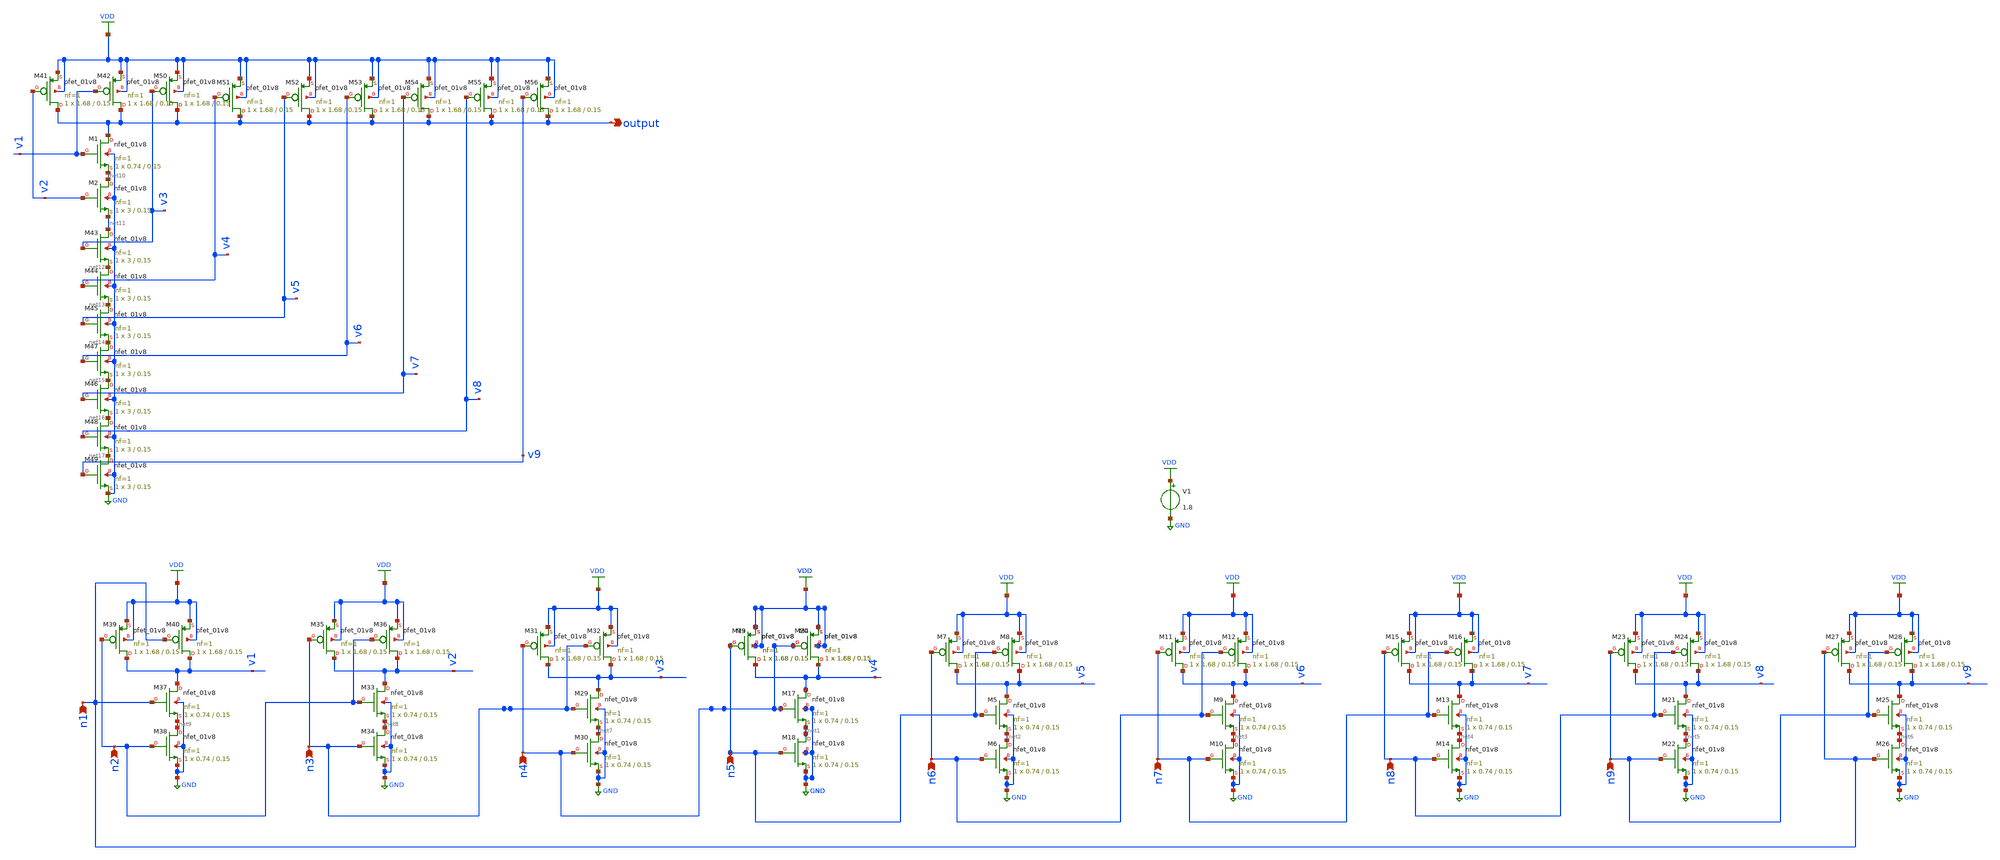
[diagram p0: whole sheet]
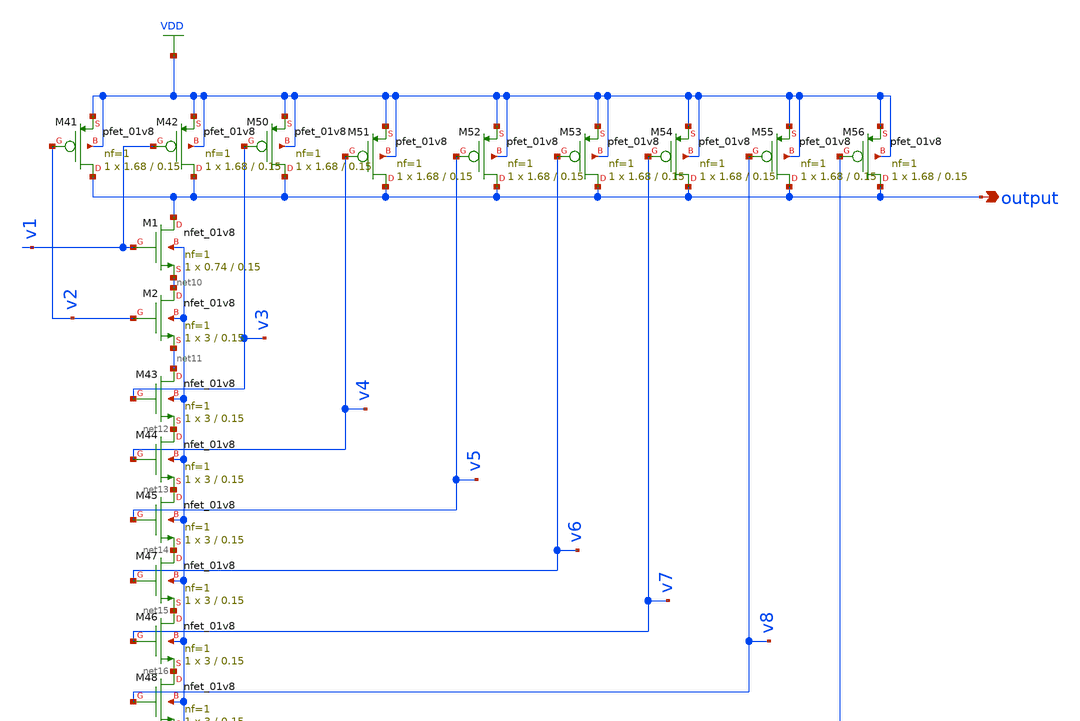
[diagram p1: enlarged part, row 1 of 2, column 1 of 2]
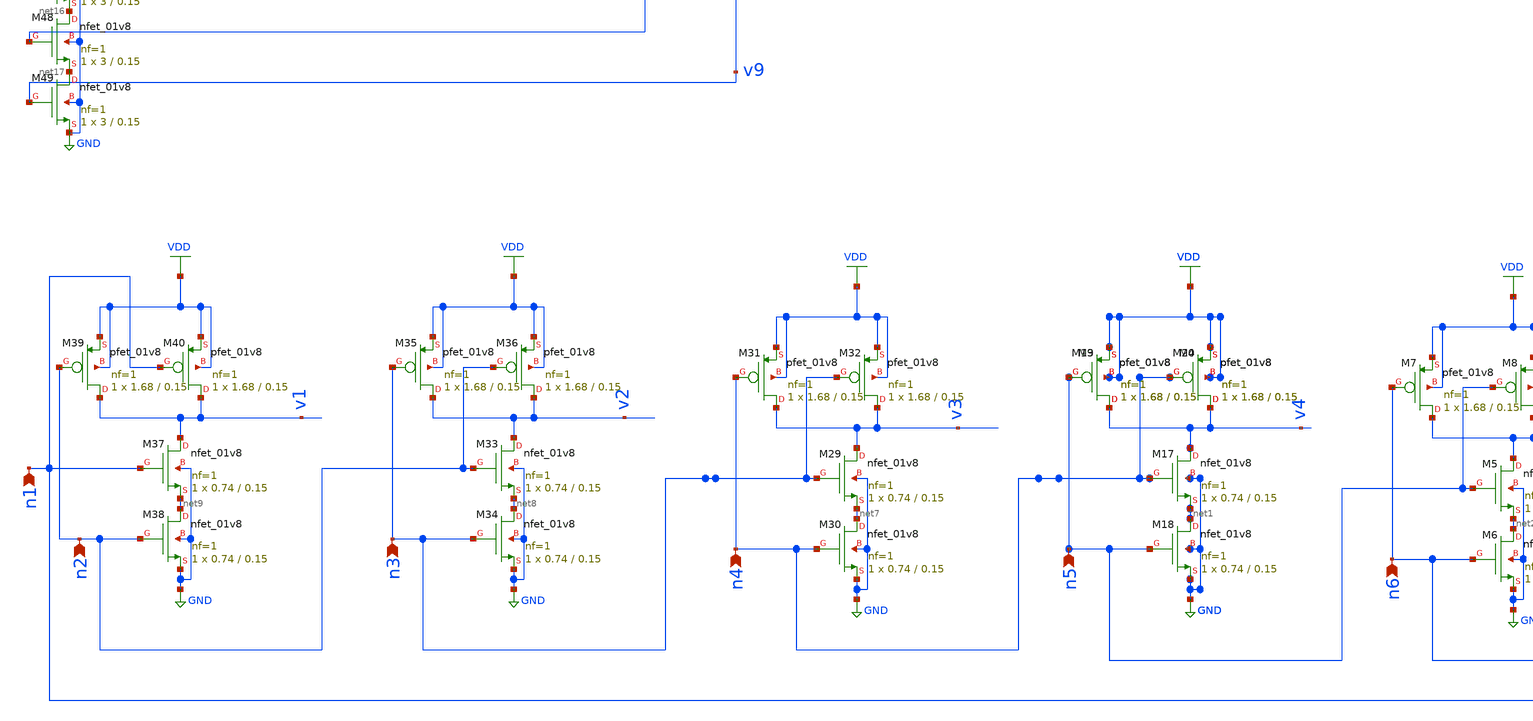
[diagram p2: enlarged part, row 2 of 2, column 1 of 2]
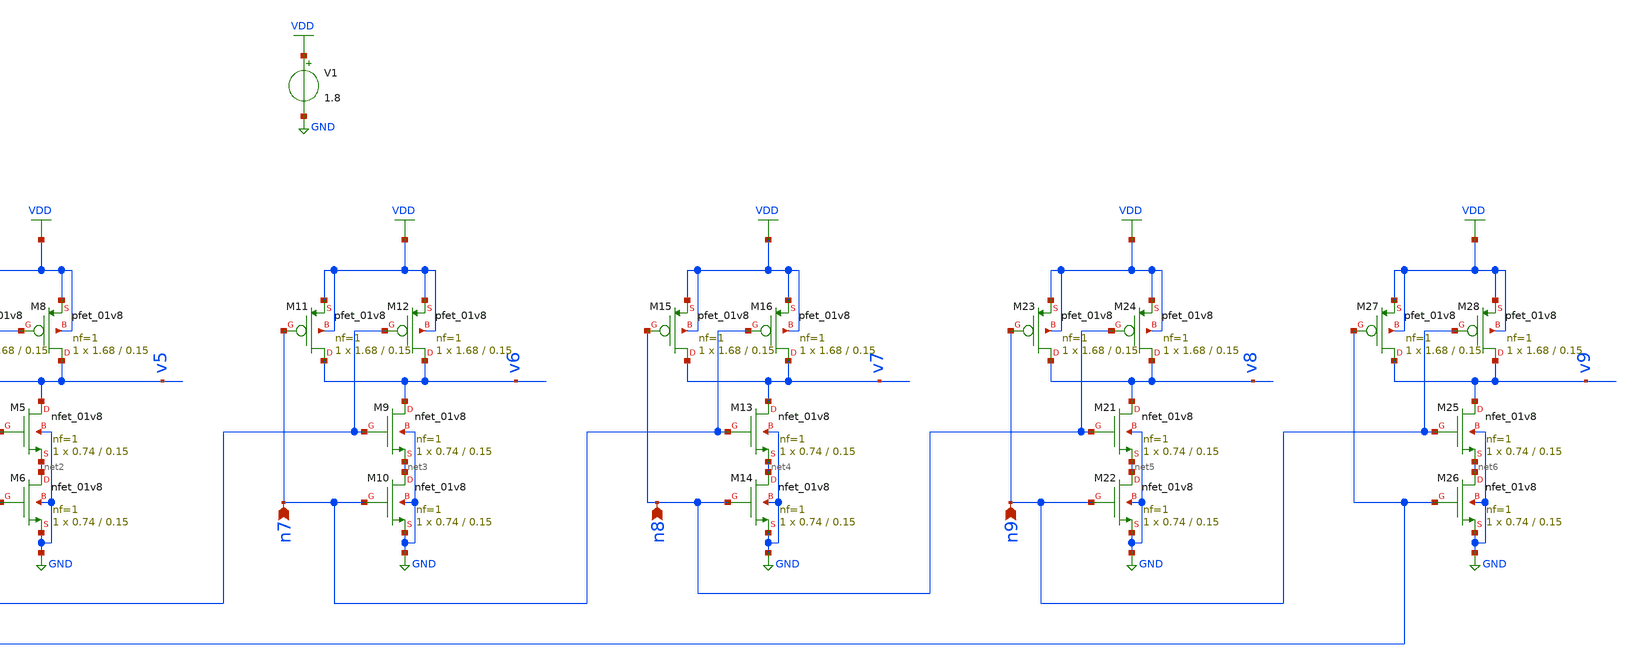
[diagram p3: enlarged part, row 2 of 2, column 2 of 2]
** sch_path: edgecombiner.sch
**.subckt edgecombiner n1 n2 n3 n4 n5 n6 n7 n8 n9 output
*.ipin n1
*.ipin n2
*.ipin n3
*.ipin n4
*.ipin n5
*.ipin n6
*.ipin n7
*.ipin n8
*.ipin n9
*.opin output
XM3 v4 n5 VDD VDD sky130_fd_pr__pfet_01v8 L=0.15 W=1.68 nf=1 ad='int((nf+1)/2) * W/nf * 0.29' as='int((nf+2)/2) * W/nf * 0.29'
+ pd='2*int((nf+1)/2) * (W/nf + 0.29)' ps='2*int((nf+2)/2) * (W/nf + 0.29)' nrd='0.29 / W' nrs='0.29 / W'
+ sa=0 sb=0 sd=0 mult=1 m=1
XM4 v4 n4 VDD VDD sky130_fd_pr__pfet_01v8 L=0.15 W=1.68 nf=1 ad='int((nf+1)/2) * W/nf * 0.29' as='int((nf+2)/2) * W/nf * 0.29'
+ pd='2*int((nf+1)/2) * (W/nf + 0.29)' ps='2*int((nf+2)/2) * (W/nf + 0.29)' nrd='0.29 / W' nrs='0.29 / W'
+ sa=0 sb=0 sd=0 mult=1 m=1
XM5 v5 n5 net2 GND sky130_fd_pr__nfet_01v8 L=0.15 W=0.74 nf=1 ad='int((nf+1)/2) * W/nf * 0.29' as='int((nf+2)/2) * W/nf * 0.29'
+ pd='2*int((nf+1)/2) * (W/nf + 0.29)' ps='2*int((nf+2)/2) * (W/nf + 0.29)' nrd='0.29 / W' nrs='0.29 / W'
+ sa=0 sb=0 sd=0 mult=1 m=1
XM6 net2 n6 GND GND sky130_fd_pr__nfet_01v8 L=0.15 W=0.74 nf=1 ad='int((nf+1)/2) * W/nf * 0.29' as='int((nf+2)/2) * W/nf * 0.29'
+ pd='2*int((nf+1)/2) * (W/nf + 0.29)' ps='2*int((nf+2)/2) * (W/nf + 0.29)' nrd='0.29 / W' nrs='0.29 / W'
+ sa=0 sb=0 sd=0 mult=1 m=1
XM7 v5 n6 VDD VDD sky130_fd_pr__pfet_01v8 L=0.15 W=1.68 nf=1 ad='int((nf+1)/2) * W/nf * 0.29' as='int((nf+2)/2) * W/nf * 0.29'
+ pd='2*int((nf+1)/2) * (W/nf + 0.29)' ps='2*int((nf+2)/2) * (W/nf + 0.29)' nrd='0.29 / W' nrs='0.29 / W'
+ sa=0 sb=0 sd=0 mult=1 m=1
XM8 v5 n5 VDD VDD sky130_fd_pr__pfet_01v8 L=0.15 W=1.68 nf=1 ad='int((nf+1)/2) * W/nf * 0.29' as='int((nf+2)/2) * W/nf * 0.29'
+ pd='2*int((nf+1)/2) * (W/nf + 0.29)' ps='2*int((nf+2)/2) * (W/nf + 0.29)' nrd='0.29 / W' nrs='0.29 / W'
+ sa=0 sb=0 sd=0 mult=1 m=1
XM9 v6 n6 net3 GND sky130_fd_pr__nfet_01v8 L=0.15 W=0.74 nf=1 ad='int((nf+1)/2) * W/nf * 0.29' as='int((nf+2)/2) * W/nf * 0.29'
+ pd='2*int((nf+1)/2) * (W/nf + 0.29)' ps='2*int((nf+2)/2) * (W/nf + 0.29)' nrd='0.29 / W' nrs='0.29 / W'
+ sa=0 sb=0 sd=0 mult=1 m=1
XM10 net3 n7 GND GND sky130_fd_pr__nfet_01v8 L=0.15 W=0.74 nf=1 ad='int((nf+1)/2) * W/nf * 0.29' as='int((nf+2)/2) * W/nf * 0.29'
+ pd='2*int((nf+1)/2) * (W/nf + 0.29)' ps='2*int((nf+2)/2) * (W/nf + 0.29)' nrd='0.29 / W' nrs='0.29 / W'
+ sa=0 sb=0 sd=0 mult=1 m=1
XM11 v6 n7 VDD VDD sky130_fd_pr__pfet_01v8 L=0.15 W=1.68 nf=1 ad='int((nf+1)/2) * W/nf * 0.29' as='int((nf+2)/2) * W/nf * 0.29'
+ pd='2*int((nf+1)/2) * (W/nf + 0.29)' ps='2*int((nf+2)/2) * (W/nf + 0.29)' nrd='0.29 / W' nrs='0.29 / W'
+ sa=0 sb=0 sd=0 mult=1 m=1
XM12 v6 n6 VDD VDD sky130_fd_pr__pfet_01v8 L=0.15 W=1.68 nf=1 ad='int((nf+1)/2) * W/nf * 0.29' as='int((nf+2)/2) * W/nf * 0.29'
+ pd='2*int((nf+1)/2) * (W/nf + 0.29)' ps='2*int((nf+2)/2) * (W/nf + 0.29)' nrd='0.29 / W' nrs='0.29 / W'
+ sa=0 sb=0 sd=0 mult=1 m=1
XM13 v7 n7 net4 GND sky130_fd_pr__nfet_01v8 L=0.15 W=0.74 nf=1 ad='int((nf+1)/2) * W/nf * 0.29' as='int((nf+2)/2) * W/nf * 0.29'
+ pd='2*int((nf+1)/2) * (W/nf + 0.29)' ps='2*int((nf+2)/2) * (W/nf + 0.29)' nrd='0.29 / W' nrs='0.29 / W'
+ sa=0 sb=0 sd=0 mult=1 m=1
XM14 net4 n8 GND GND sky130_fd_pr__nfet_01v8 L=0.15 W=0.74 nf=1 ad='int((nf+1)/2) * W/nf * 0.29' as='int((nf+2)/2) * W/nf * 0.29'
+ pd='2*int((nf+1)/2) * (W/nf + 0.29)' ps='2*int((nf+2)/2) * (W/nf + 0.29)' nrd='0.29 / W' nrs='0.29 / W'
+ sa=0 sb=0 sd=0 mult=1 m=1
XM15 v7 n8 VDD VDD sky130_fd_pr__pfet_01v8 L=0.15 W=1.68 nf=1 ad='int((nf+1)/2) * W/nf * 0.29' as='int((nf+2)/2) * W/nf * 0.29'
+ pd='2*int((nf+1)/2) * (W/nf + 0.29)' ps='2*int((nf+2)/2) * (W/nf + 0.29)' nrd='0.29 / W' nrs='0.29 / W'
+ sa=0 sb=0 sd=0 mult=1 m=1
XM16 v7 n7 VDD VDD sky130_fd_pr__pfet_01v8 L=0.15 W=1.68 nf=1 ad='int((nf+1)/2) * W/nf * 0.29' as='int((nf+2)/2) * W/nf * 0.29'
+ pd='2*int((nf+1)/2) * (W/nf + 0.29)' ps='2*int((nf+2)/2) * (W/nf + 0.29)' nrd='0.29 / W' nrs='0.29 / W'
+ sa=0 sb=0 sd=0 mult=1 m=1
XM17 v4 n4 net1 GND sky130_fd_pr__nfet_01v8 L=0.15 W=0.74 nf=1 ad='int((nf+1)/2) * W/nf * 0.29' as='int((nf+2)/2) * W/nf * 0.29'
+ pd='2*int((nf+1)/2) * (W/nf + 0.29)' ps='2*int((nf+2)/2) * (W/nf + 0.29)' nrd='0.29 / W' nrs='0.29 / W'
+ sa=0 sb=0 sd=0 mult=1 m=1
XM18 net1 n5 GND GND sky130_fd_pr__nfet_01v8 L=0.15 W=0.74 nf=1 ad='int((nf+1)/2) * W/nf * 0.29' as='int((nf+2)/2) * W/nf * 0.29'
+ pd='2*int((nf+1)/2) * (W/nf + 0.29)' ps='2*int((nf+2)/2) * (W/nf + 0.29)' nrd='0.29 / W' nrs='0.29 / W'
+ sa=0 sb=0 sd=0 mult=1 m=1
XM19 v4 n5 VDD VDD sky130_fd_pr__pfet_01v8 L=0.15 W=1.68 nf=1 ad='int((nf+1)/2) * W/nf * 0.29' as='int((nf+2)/2) * W/nf * 0.29'
+ pd='2*int((nf+1)/2) * (W/nf + 0.29)' ps='2*int((nf+2)/2) * (W/nf + 0.29)' nrd='0.29 / W' nrs='0.29 / W'
+ sa=0 sb=0 sd=0 mult=1 m=1
XM20 v4 n4 VDD VDD sky130_fd_pr__pfet_01v8 L=0.15 W=1.68 nf=1 ad='int((nf+1)/2) * W/nf * 0.29' as='int((nf+2)/2) * W/nf * 0.29'
+ pd='2*int((nf+1)/2) * (W/nf + 0.29)' ps='2*int((nf+2)/2) * (W/nf + 0.29)' nrd='0.29 / W' nrs='0.29 / W'
+ sa=0 sb=0 sd=0 mult=1 m=1
XM21 v8 n8 net5 GND sky130_fd_pr__nfet_01v8 L=0.15 W=0.74 nf=1 ad='int((nf+1)/2) * W/nf * 0.29' as='int((nf+2)/2) * W/nf * 0.29'
+ pd='2*int((nf+1)/2) * (W/nf + 0.29)' ps='2*int((nf+2)/2) * (W/nf + 0.29)' nrd='0.29 / W' nrs='0.29 / W'
+ sa=0 sb=0 sd=0 mult=1 m=1
XM22 net5 n9 GND GND sky130_fd_pr__nfet_01v8 L=0.15 W=0.74 nf=1 ad='int((nf+1)/2) * W/nf * 0.29' as='int((nf+2)/2) * W/nf * 0.29'
+ pd='2*int((nf+1)/2) * (W/nf + 0.29)' ps='2*int((nf+2)/2) * (W/nf + 0.29)' nrd='0.29 / W' nrs='0.29 / W'
+ sa=0 sb=0 sd=0 mult=1 m=1
XM23 v8 n9 VDD VDD sky130_fd_pr__pfet_01v8 L=0.15 W=1.68 nf=1 ad='int((nf+1)/2) * W/nf * 0.29' as='int((nf+2)/2) * W/nf * 0.29'
+ pd='2*int((nf+1)/2) * (W/nf + 0.29)' ps='2*int((nf+2)/2) * (W/nf + 0.29)' nrd='0.29 / W' nrs='0.29 / W'
+ sa=0 sb=0 sd=0 mult=1 m=1
XM24 v8 n8 VDD VDD sky130_fd_pr__pfet_01v8 L=0.15 W=1.68 nf=1 ad='int((nf+1)/2) * W/nf * 0.29' as='int((nf+2)/2) * W/nf * 0.29'
+ pd='2*int((nf+1)/2) * (W/nf + 0.29)' ps='2*int((nf+2)/2) * (W/nf + 0.29)' nrd='0.29 / W' nrs='0.29 / W'
+ sa=0 sb=0 sd=0 mult=1 m=1
XM25 v9 n9 net6 GND sky130_fd_pr__nfet_01v8 L=0.15 W=0.74 nf=1 ad='int((nf+1)/2) * W/nf * 0.29' as='int((nf+2)/2) * W/nf * 0.29'
+ pd='2*int((nf+1)/2) * (W/nf + 0.29)' ps='2*int((nf+2)/2) * (W/nf + 0.29)' nrd='0.29 / W' nrs='0.29 / W'
+ sa=0 sb=0 sd=0 mult=1 m=1
XM26 net6 n1 GND GND sky130_fd_pr__nfet_01v8 L=0.15 W=0.74 nf=1 ad='int((nf+1)/2) * W/nf * 0.29' as='int((nf+2)/2) * W/nf * 0.29'
+ pd='2*int((nf+1)/2) * (W/nf + 0.29)' ps='2*int((nf+2)/2) * (W/nf + 0.29)' nrd='0.29 / W' nrs='0.29 / W'
+ sa=0 sb=0 sd=0 mult=1 m=1
XM27 v9 n1 VDD VDD sky130_fd_pr__pfet_01v8 L=0.15 W=1.68 nf=1 ad='int((nf+1)/2) * W/nf * 0.29' as='int((nf+2)/2) * W/nf * 0.29'
+ pd='2*int((nf+1)/2) * (W/nf + 0.29)' ps='2*int((nf+2)/2) * (W/nf + 0.29)' nrd='0.29 / W' nrs='0.29 / W'
+ sa=0 sb=0 sd=0 mult=1 m=1
XM28 v9 n9 VDD VDD sky130_fd_pr__pfet_01v8 L=0.15 W=1.68 nf=1 ad='int((nf+1)/2) * W/nf * 0.29' as='int((nf+2)/2) * W/nf * 0.29'
+ pd='2*int((nf+1)/2) * (W/nf + 0.29)' ps='2*int((nf+2)/2) * (W/nf + 0.29)' nrd='0.29 / W' nrs='0.29 / W'
+ sa=0 sb=0 sd=0 mult=1 m=1
XM29 v3 n3 net7 GND sky130_fd_pr__nfet_01v8 L=0.15 W=0.74 nf=1 ad='int((nf+1)/2) * W/nf * 0.29' as='int((nf+2)/2) * W/nf * 0.29'
+ pd='2*int((nf+1)/2) * (W/nf + 0.29)' ps='2*int((nf+2)/2) * (W/nf + 0.29)' nrd='0.29 / W' nrs='0.29 / W'
+ sa=0 sb=0 sd=0 mult=1 m=1
XM30 net7 n4 GND GND sky130_fd_pr__nfet_01v8 L=0.15 W=0.74 nf=1 ad='int((nf+1)/2) * W/nf * 0.29' as='int((nf+2)/2) * W/nf * 0.29'
+ pd='2*int((nf+1)/2) * (W/nf + 0.29)' ps='2*int((nf+2)/2) * (W/nf + 0.29)' nrd='0.29 / W' nrs='0.29 / W'
+ sa=0 sb=0 sd=0 mult=1 m=1
XM31 v3 n4 VDD VDD sky130_fd_pr__pfet_01v8 L=0.15 W=1.68 nf=1 ad='int((nf+1)/2) * W/nf * 0.29' as='int((nf+2)/2) * W/nf * 0.29'
+ pd='2*int((nf+1)/2) * (W/nf + 0.29)' ps='2*int((nf+2)/2) * (W/nf + 0.29)' nrd='0.29 / W' nrs='0.29 / W'
+ sa=0 sb=0 sd=0 mult=1 m=1
XM32 v3 n3 VDD VDD sky130_fd_pr__pfet_01v8 L=0.15 W=1.68 nf=1 ad='int((nf+1)/2) * W/nf * 0.29' as='int((nf+2)/2) * W/nf * 0.29'
+ pd='2*int((nf+1)/2) * (W/nf + 0.29)' ps='2*int((nf+2)/2) * (W/nf + 0.29)' nrd='0.29 / W' nrs='0.29 / W'
+ sa=0 sb=0 sd=0 mult=1 m=1
XM33 v2 n2 net8 GND sky130_fd_pr__nfet_01v8 L=0.15 W=0.74 nf=1 ad='int((nf+1)/2) * W/nf * 0.29' as='int((nf+2)/2) * W/nf * 0.29'
+ pd='2*int((nf+1)/2) * (W/nf + 0.29)' ps='2*int((nf+2)/2) * (W/nf + 0.29)' nrd='0.29 / W' nrs='0.29 / W'
+ sa=0 sb=0 sd=0 mult=1 m=1
XM34 net8 n3 GND GND sky130_fd_pr__nfet_01v8 L=0.15 W=0.74 nf=1 ad='int((nf+1)/2) * W/nf * 0.29' as='int((nf+2)/2) * W/nf * 0.29'
+ pd='2*int((nf+1)/2) * (W/nf + 0.29)' ps='2*int((nf+2)/2) * (W/nf + 0.29)' nrd='0.29 / W' nrs='0.29 / W'
+ sa=0 sb=0 sd=0 mult=1 m=1
XM35 v2 n3 VDD VDD sky130_fd_pr__pfet_01v8 L=0.15 W=1.68 nf=1 ad='int((nf+1)/2) * W/nf * 0.29' as='int((nf+2)/2) * W/nf * 0.29'
+ pd='2*int((nf+1)/2) * (W/nf + 0.29)' ps='2*int((nf+2)/2) * (W/nf + 0.29)' nrd='0.29 / W' nrs='0.29 / W'
+ sa=0 sb=0 sd=0 mult=1 m=1
XM36 v2 n2 VDD VDD sky130_fd_pr__pfet_01v8 L=0.15 W=1.68 nf=1 ad='int((nf+1)/2) * W/nf * 0.29' as='int((nf+2)/2) * W/nf * 0.29'
+ pd='2*int((nf+1)/2) * (W/nf + 0.29)' ps='2*int((nf+2)/2) * (W/nf + 0.29)' nrd='0.29 / W' nrs='0.29 / W'
+ sa=0 sb=0 sd=0 mult=1 m=1
XM37 v1 n1 net9 GND sky130_fd_pr__nfet_01v8 L=0.15 W=0.74 nf=1 ad='int((nf+1)/2) * W/nf * 0.29' as='int((nf+2)/2) * W/nf * 0.29'
+ pd='2*int((nf+1)/2) * (W/nf + 0.29)' ps='2*int((nf+2)/2) * (W/nf + 0.29)' nrd='0.29 / W' nrs='0.29 / W'
+ sa=0 sb=0 sd=0 mult=1 m=1
XM38 net9 n2 GND GND sky130_fd_pr__nfet_01v8 L=0.15 W=0.74 nf=1 ad='int((nf+1)/2) * W/nf * 0.29' as='int((nf+2)/2) * W/nf * 0.29'
+ pd='2*int((nf+1)/2) * (W/nf + 0.29)' ps='2*int((nf+2)/2) * (W/nf + 0.29)' nrd='0.29 / W' nrs='0.29 / W'
+ sa=0 sb=0 sd=0 mult=1 m=1
XM39 v1 n2 VDD VDD sky130_fd_pr__pfet_01v8 L=0.15 W=1.68 nf=1 ad='int((nf+1)/2) * W/nf * 0.29' as='int((nf+2)/2) * W/nf * 0.29'
+ pd='2*int((nf+1)/2) * (W/nf + 0.29)' ps='2*int((nf+2)/2) * (W/nf + 0.29)' nrd='0.29 / W' nrs='0.29 / W'
+ sa=0 sb=0 sd=0 mult=1 m=1
XM40 v1 n1 VDD VDD sky130_fd_pr__pfet_01v8 L=0.15 W=1.68 nf=1 ad='int((nf+1)/2) * W/nf * 0.29' as='int((nf+2)/2) * W/nf * 0.29'
+ pd='2*int((nf+1)/2) * (W/nf + 0.29)' ps='2*int((nf+2)/2) * (W/nf + 0.29)' nrd='0.29 / W' nrs='0.29 / W'
+ sa=0 sb=0 sd=0 mult=1 m=1
V1 VDD GND 1.8
XM1 output v1 net10 GND sky130_fd_pr__nfet_01v8 L=0.15 W=0.74 nf=1 ad='int((nf+1)/2) * W/nf * 0.29' as='int((nf+2)/2) * W/nf * 0.29'
+ pd='2*int((nf+1)/2) * (W/nf + 0.29)' ps='2*int((nf+2)/2) * (W/nf + 0.29)' nrd='0.29 / W' nrs='0.29 / W'
+ sa=0 sb=0 sd=0 mult=1 m=1
XM2 net10 v2 net11 GND sky130_fd_pr__nfet_01v8 L=0.15 W=3 nf=1 ad='int((nf+1)/2) * W/nf * 0.29' as='int((nf+2)/2) * W/nf * 0.29'
+ pd='2*int((nf+1)/2) * (W/nf + 0.29)' ps='2*int((nf+2)/2) * (W/nf + 0.29)' nrd='0.29 / W' nrs='0.29 / W'
+ sa=0 sb=0 sd=0 mult=1 m=1
XM41 output v2 VDD VDD sky130_fd_pr__pfet_01v8 L=0.15 W=1.68 nf=1 ad='int((nf+1)/2) * W/nf * 0.29' as='int((nf+2)/2) * W/nf * 0.29'
+ pd='2*int((nf+1)/2) * (W/nf + 0.29)' ps='2*int((nf+2)/2) * (W/nf + 0.29)' nrd='0.29 / W' nrs='0.29 / W'
+ sa=0 sb=0 sd=0 mult=1 m=1
XM42 output v1 VDD VDD sky130_fd_pr__pfet_01v8 L=0.15 W=1.68 nf=1 ad='int((nf+1)/2) * W/nf * 0.29' as='int((nf+2)/2) * W/nf * 0.29'
+ pd='2*int((nf+1)/2) * (W/nf + 0.29)' ps='2*int((nf+2)/2) * (W/nf + 0.29)' nrd='0.29 / W' nrs='0.29 / W'
+ sa=0 sb=0 sd=0 mult=1 m=1
XM43 net11 v3 net12 GND sky130_fd_pr__nfet_01v8 L=0.15 W=3 nf=1 ad='int((nf+1)/2) * W/nf * 0.29' as='int((nf+2)/2) * W/nf * 0.29'
+ pd='2*int((nf+1)/2) * (W/nf + 0.29)' ps='2*int((nf+2)/2) * (W/nf + 0.29)' nrd='0.29 / W' nrs='0.29 / W'
+ sa=0 sb=0 sd=0 mult=1 m=1
XM44 net12 v4 net13 GND sky130_fd_pr__nfet_01v8 L=0.15 W=3 nf=1 ad='int((nf+1)/2) * W/nf * 0.29' as='int((nf+2)/2) * W/nf * 0.29'
+ pd='2*int((nf+1)/2) * (W/nf + 0.29)' ps='2*int((nf+2)/2) * (W/nf + 0.29)' nrd='0.29 / W' nrs='0.29 / W'
+ sa=0 sb=0 sd=0 mult=1 m=1
XM45 net13 v5 net14 GND sky130_fd_pr__nfet_01v8 L=0.15 W=3 nf=1 ad='int((nf+1)/2) * W/nf * 0.29' as='int((nf+2)/2) * W/nf * 0.29'
+ pd='2*int((nf+1)/2) * (W/nf + 0.29)' ps='2*int((nf+2)/2) * (W/nf + 0.29)' nrd='0.29 / W' nrs='0.29 / W'
+ sa=0 sb=0 sd=0 mult=1 m=1
XM46 net15 v7 net16 GND sky130_fd_pr__nfet_01v8 L=0.15 W=3 nf=1 ad='int((nf+1)/2) * W/nf * 0.29' as='int((nf+2)/2) * W/nf * 0.29'
+ pd='2*int((nf+1)/2) * (W/nf + 0.29)' ps='2*int((nf+2)/2) * (W/nf + 0.29)' nrd='0.29 / W' nrs='0.29 / W'
+ sa=0 sb=0 sd=0 mult=1 m=1
XM47 net14 v6 net15 GND sky130_fd_pr__nfet_01v8 L=0.15 W=3 nf=1 ad='int((nf+1)/2) * W/nf * 0.29' as='int((nf+2)/2) * W/nf * 0.29'
+ pd='2*int((nf+1)/2) * (W/nf + 0.29)' ps='2*int((nf+2)/2) * (W/nf + 0.29)' nrd='0.29 / W' nrs='0.29 / W'
+ sa=0 sb=0 sd=0 mult=1 m=1
XM48 net16 v8 net17 GND sky130_fd_pr__nfet_01v8 L=0.15 W=3 nf=1 ad='int((nf+1)/2) * W/nf * 0.29' as='int((nf+2)/2) * W/nf * 0.29'
+ pd='2*int((nf+1)/2) * (W/nf + 0.29)' ps='2*int((nf+2)/2) * (W/nf + 0.29)' nrd='0.29 / W' nrs='0.29 / W'
+ sa=0 sb=0 sd=0 mult=1 m=1
XM49 net17 v9 GND GND sky130_fd_pr__nfet_01v8 L=0.15 W=3 nf=1 ad='int((nf+1)/2) * W/nf * 0.29' as='int((nf+2)/2) * W/nf * 0.29'
+ pd='2*int((nf+1)/2) * (W/nf + 0.29)' ps='2*int((nf+2)/2) * (W/nf + 0.29)' nrd='0.29 / W' nrs='0.29 / W'
+ sa=0 sb=0 sd=0 mult=1 m=1
XM51 output v4 VDD VDD sky130_fd_pr__pfet_01v8 L=0.15 W=1.68 nf=1 ad='int((nf+1)/2) * W/nf * 0.29' as='int((nf+2)/2) * W/nf * 0.29'
+ pd='2*int((nf+1)/2) * (W/nf + 0.29)' ps='2*int((nf+2)/2) * (W/nf + 0.29)' nrd='0.29 / W' nrs='0.29 / W'
+ sa=0 sb=0 sd=0 mult=1 m=1
XM52 output v5 VDD VDD sky130_fd_pr__pfet_01v8 L=0.15 W=1.68 nf=1 ad='int((nf+1)/2) * W/nf * 0.29' as='int((nf+2)/2) * W/nf * 0.29'
+ pd='2*int((nf+1)/2) * (W/nf + 0.29)' ps='2*int((nf+2)/2) * (W/nf + 0.29)' nrd='0.29 / W' nrs='0.29 / W'
+ sa=0 sb=0 sd=0 mult=1 m=1
XM53 output v6 VDD VDD sky130_fd_pr__pfet_01v8 L=0.15 W=1.68 nf=1 ad='int((nf+1)/2) * W/nf * 0.29' as='int((nf+2)/2) * W/nf * 0.29'
+ pd='2*int((nf+1)/2) * (W/nf + 0.29)' ps='2*int((nf+2)/2) * (W/nf + 0.29)' nrd='0.29 / W' nrs='0.29 / W'
+ sa=0 sb=0 sd=0 mult=1 m=1
XM54 output v7 VDD VDD sky130_fd_pr__pfet_01v8 L=0.15 W=1.68 nf=1 ad='int((nf+1)/2) * W/nf * 0.29' as='int((nf+2)/2) * W/nf * 0.29'
+ pd='2*int((nf+1)/2) * (W/nf + 0.29)' ps='2*int((nf+2)/2) * (W/nf + 0.29)' nrd='0.29 / W' nrs='0.29 / W'
+ sa=0 sb=0 sd=0 mult=1 m=1
XM55 output v8 VDD VDD sky130_fd_pr__pfet_01v8 L=0.15 W=1.68 nf=1 ad='int((nf+1)/2) * W/nf * 0.29' as='int((nf+2)/2) * W/nf * 0.29'
+ pd='2*int((nf+1)/2) * (W/nf + 0.29)' ps='2*int((nf+2)/2) * (W/nf + 0.29)' nrd='0.29 / W' nrs='0.29 / W'
+ sa=0 sb=0 sd=0 mult=1 m=1
XM56 output v9 VDD VDD sky130_fd_pr__pfet_01v8 L=0.15 W=1.68 nf=1 ad='int((nf+1)/2) * W/nf * 0.29' as='int((nf+2)/2) * W/nf * 0.29'
+ pd='2*int((nf+1)/2) * (W/nf + 0.29)' ps='2*int((nf+2)/2) * (W/nf + 0.29)' nrd='0.29 / W' nrs='0.29 / W'
+ sa=0 sb=0 sd=0 mult=1 m=1
XM50 output v3 VDD VDD sky130_fd_pr__pfet_01v8 L=0.15 W=1.68 nf=1 ad='int((nf+1)/2) * W/nf * 0.29' as='int((nf+2)/2) * W/nf * 0.29'
+ pd='2*int((nf+1)/2) * (W/nf + 0.29)' ps='2*int((nf+2)/2) * (W/nf + 0.29)' nrd='0.29 / W' nrs='0.29 / W'
+ sa=0 sb=0 sd=0 mult=1 m=1
**.ends
.GLOBAL VDD
.GLOBAL GND
.end
